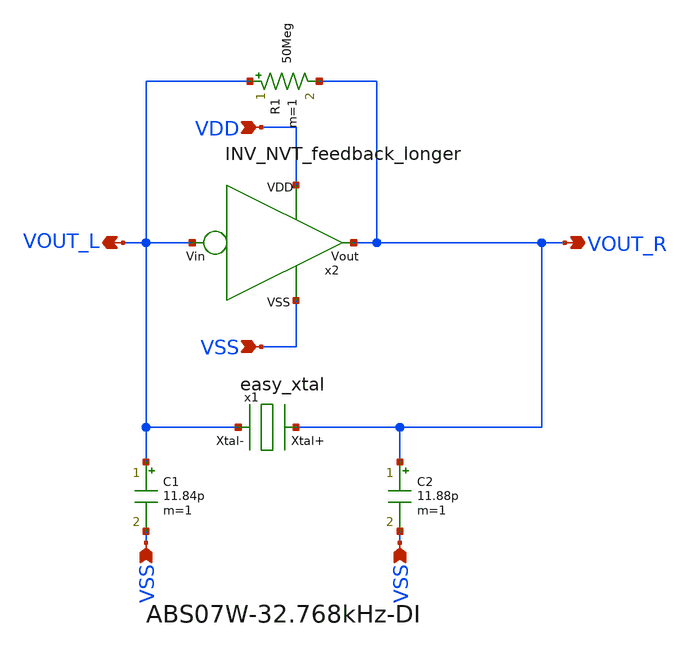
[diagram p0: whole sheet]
** sch_path: design/THESIS_EXP_RO_INVERTER_SKY130A/xtal_osc_NVT_LL.sch
**.subckt xtal_osc_NVT_LL VSS VSS VOUT_R VOUT_L VDD VSS
*.ipin VSS
*.ipin VSS
*.opin VOUT_R
*.opin VOUT_L
*.ipin VDD
*.ipin VSS
C1 VOUT_L VSS 11.84p m=1
C2 VOUT_R VSS 11.88p m=1
R1 VOUT_L VOUT_R 50Meg m=1
x2 VDD VSS VOUT_R VOUT_L INV_NVT_feedback_longer
x1 VOUT_R VOUT_L easy_xtal
**.ends
.end
